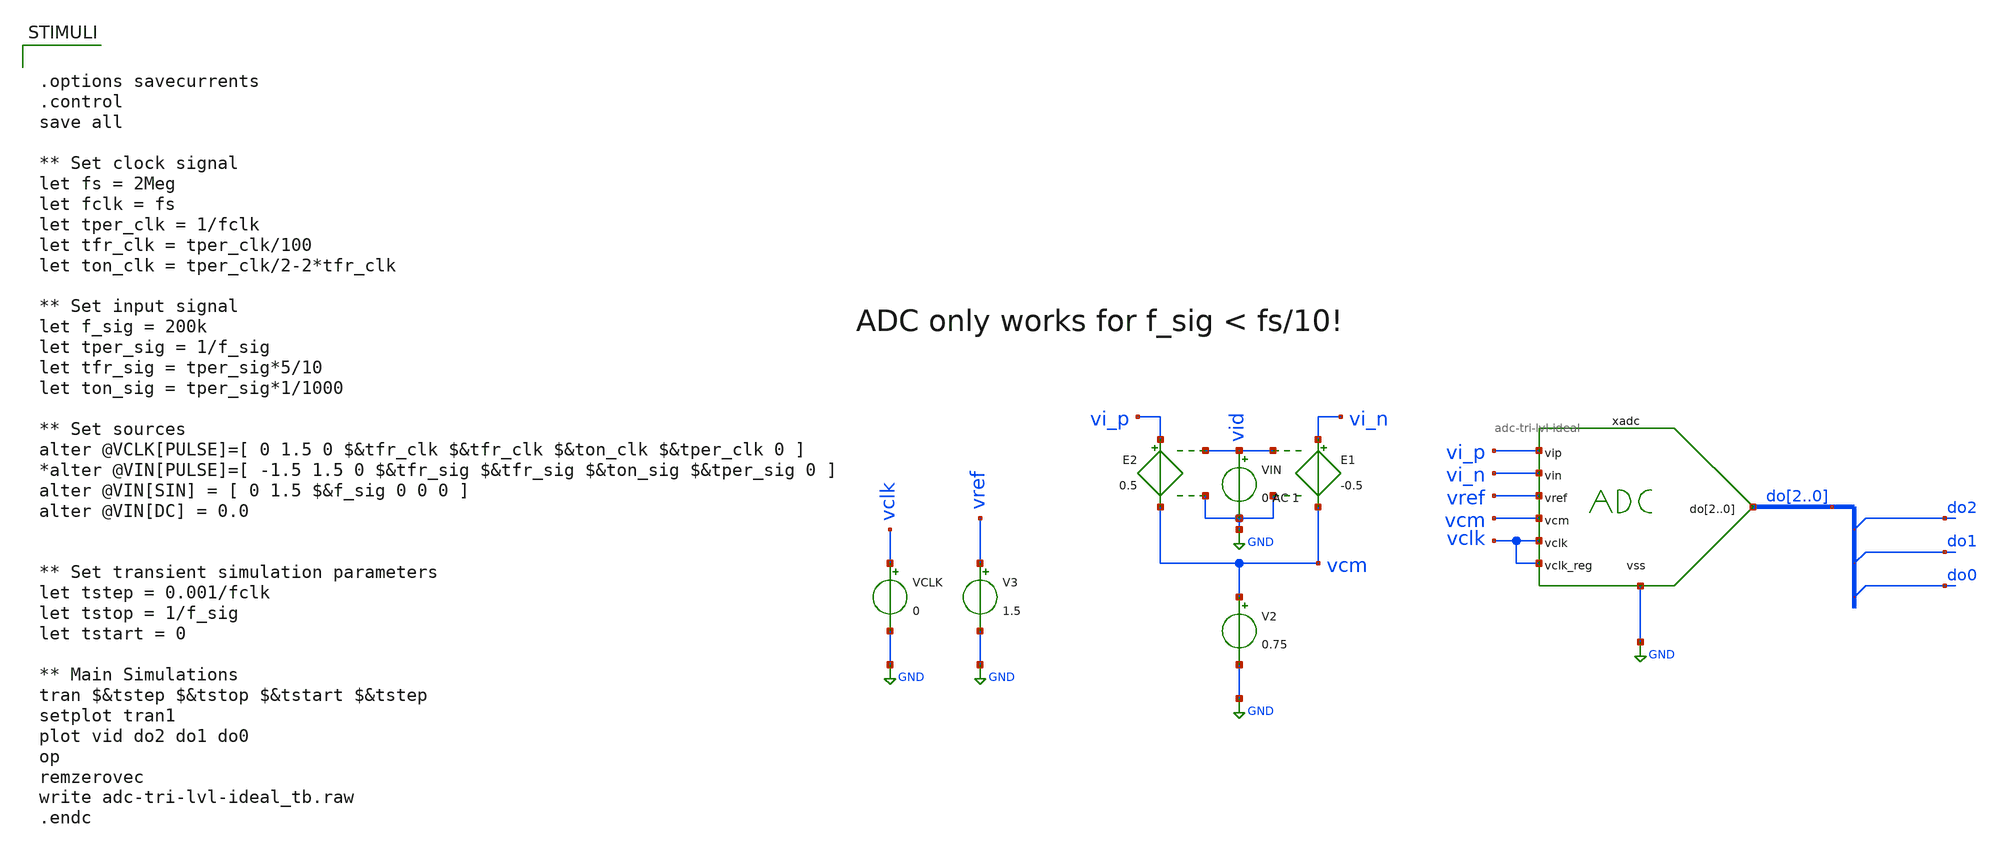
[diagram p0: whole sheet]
** sch_path: xschem/adc-tri-lvl-ideal_tb.sch
**.subckt adc-tri-lvl-ideal_tb
V2 vcm GND 0.75
E1 vi_n vcm vid GND -0.5
E2 vi_p vcm vid GND 0.5
VIN vid GND 0 AC 1
VCLK vclk GND 0
V3 vref GND 1.5
xadc do2 do1 do0 vi_p vi_n vref vcm vclk GND vclk adc-tri-lvl-ideal
**** begin user architecture code


.options savecurrents
.control
save all

** Set clock signal
let fs = 2Meg
let fclk = fs
let tper_clk = 1/fclk
let tfr_clk = tper_clk/100
let ton_clk = tper_clk/2-2*tfr_clk

** Set input signal
let f_sig = 200k
let tper_sig = 1/f_sig
let tfr_sig = tper_sig*5/10
let ton_sig = tper_sig*1/1000

** Set sources
alter @VCLK[PULSE]=[ 0 1.5 0 $&tfr_clk $&tfr_clk $&ton_clk $&tper_clk 0 ]
*alter @VIN[PULSE]=[ -1.5 1.5 0 $&tfr_sig $&tfr_sig $&ton_sig $&tper_sig 0 ]
alter @VIN[SIN] = [ 0 1.5 $&f_sig 0 0 0 ]
alter @VIN[DC] = 0.0


** Set transient simulation parameters
let tstep = 0.001/fclk
let tstop = 1/f_sig
let tstart = 0

** Main Simulations
tran $&tstep $&tstop $&tstart $&tstep
setplot tran1
plot vid do2 do1 do0
op
remzerovec
write adc-tri-lvl-ideal_tb.raw
.endc

**** end user architecture code
**.ends

* expanding   symbol:  adc-tri-lvl-ideal.sym # of pins=8
** sym_path: xschem/adc-tri-lvl-ideal.sym
** sch_path: xschem/adc-tri-lvl-ideal.sch
.subckt adc-tri-lvl-ideal do2 do1 do0 vip vin vref vcm vclk vss vclk_reg
*.iopin vss
*.ipin vip
*.ipin vin
*.ipin vref
*.ipin vcm
*.ipin vclk
*.opin do2,do1,do0
*.ipin vclk_reg
xcomp1 D1 vip vin vcm vref vss comp-macro
xcomp2 D0 vip vin vref vcm vss comp-macro
**** begin user architecture code


a31 Q_REG0 CLK_REG NULL NULL %d(Q0 NQ0) dff1
a32 Q_REG1 CLK_REG NULL NULL %d(Q1 NQ1) dff1


**** end user architecture code
**** begin user architecture code


.model adc_buf adc_bridge(in_low=0.7499 in_high=0.7501)
.model dac1 dac_bridge(out_low = 0 out_high = 1.5 out_undef = 0 input_load = 0.1e-15 t_rise =
+ 0.01e-9 t_fall = 0.01e-9)
.model inv1 d_inverter(rise_delay = 0.01e-9 fall_delay = 0.01e-9 input_load = 0.1e-15)
.model and1 d_and(rise_delay = 0.01e-9 fall_delay = 0.01e-9 input_load = 0.01e-15)
.model dff1 d_dff(clk_delay = 0.01e-9 set_delay = 0.01e-9 reset_delay = 0.01e-9 ic = 0 rise_delay =
+ 0.01e-9 fall_delay = 0.01e-9)
.model dlatch1 d_dlatch(data_delay = 0.01e-9 enable_delay = 0.01e-9 set_delay = 0.01e-9 reset_delay
+ = 0.01e-9 ic = 0 rise_delay = 0.01e-9 fall_delay = 0.01e-9)

**** end user architecture code
A1 [ vclk ] [ CLK ] adc_buf
A3 [ H1 ] [ do1 ] dac1
A4 [ H2 ] [ do2 ] dac1
**** begin user architecture code


a23 [NQ1 Q0] %d(H0) and1
a24 [NQ1 NQ0] %d(H1) and1
a25 [Q1 Q0] %d(H2) and1


**** end user architecture code
A2 [ H0 ] [ do0 ] dac1
**** begin user architecture code


a21 D0 CLK NULL NULL %d(Q_REG0 NQ_REG0) dlatch1
a22 D1 CLK NULL NULL %d(Q_REG1 NQ_REG1) dlatch1


**** end user architecture code
A5 [ vclk_reg ] [ CLK_REG ] adc_buf
.ends


* expanding   symbol:  comp-macro.sym # of pins=6
** sym_path: xschem/comp-macro.sym
** sch_path: xschem/comp-macro.sch
.subckt comp-macro do vip_1 vin_1 vip_2 vin_2 vss
*.iopin vss
*.ipin vip_1
*.ipin vin_1
*.ipin vip_2
*.ipin vin_2
*.opin do
A1 [ net1 ] [ do ] comp0
E1 net1 net2 vip_1 vin_1 1
E2 net2 vss vip_2 vin_2 1
**** begin user architecture code

.model comp0 adc_bridge(in_low=-0.0001 in_high=0.0001)

**** end user architecture code
.ends

.GLOBAL GND
.end
